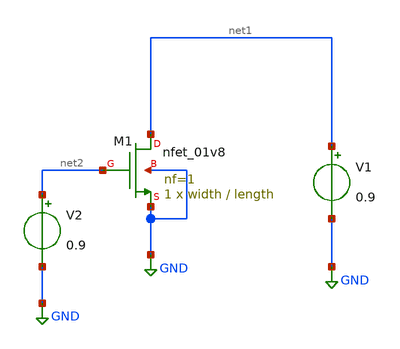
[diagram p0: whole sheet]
** sch_path: NMOS_Charac/nmos_gmid.sch
**.subckt nmos_gmid
V1 net1 GND 0.9
V2 net2 GND 0.9
XM1 net1 net2 GND GND sky130_fd_pr__nfet_01v8 L=length W=width nf=1 ad='int((nf+1)/2) * W/nf * 0.29'
+ as='int((nf+2)/2) * W/nf * 0.29' pd='2*int((nf+1)/2) * (W/nf + 0.29)' ps='2*int((nf+2)/2) * (W/nf + 0.29)'
+ nrd='0.29 / W' nrs='0.29 / W' sa=0 sb=0 sd=0 mult=1 m=1
**** begin user architecture code



.include init.txt
.include nmos_params.txt
.include to_file.txt

.param length = 0.15
.param width = 1




**** end user architecture code
**.ends
.GLOBAL GND
.end
